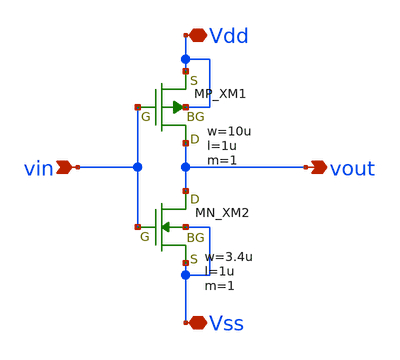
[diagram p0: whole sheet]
** sch_path: member_project/inverter/ZEP/cat_nekonekone/inverter_cat_nekonekone.sch
**.subckt inverter_cat_nekonekone vin vout Vdd Vss
*.ipin vin
*.opin vout
*.iopin Vdd
*.iopin Vss
XXM1 vout vin Vdd Vdd PMOS w=10u l=1u nrd=0 nrs=0 m=1
XXM2 vout vin Vss Vss NMOS w=3.4u l=1u nrd=0 nrs=0 m=1
**.ends
.end
